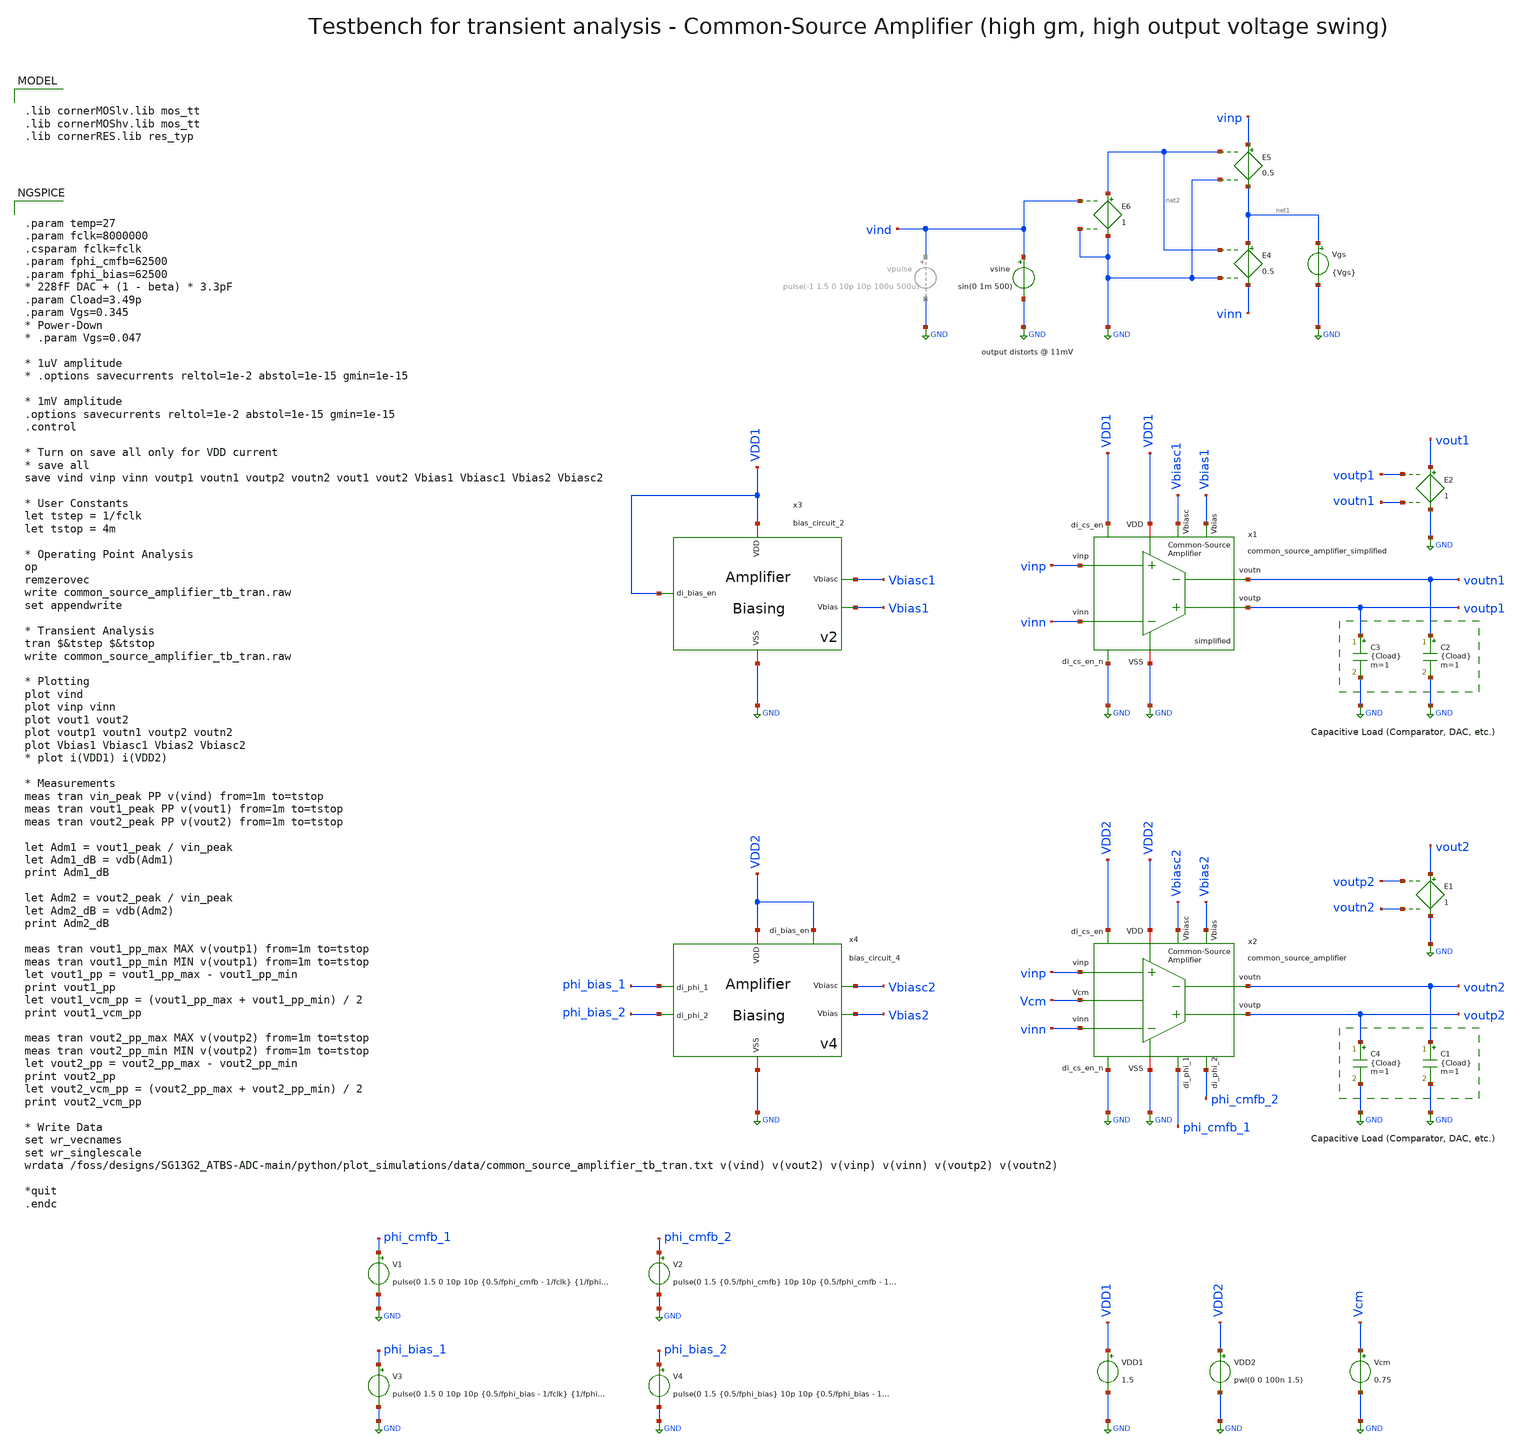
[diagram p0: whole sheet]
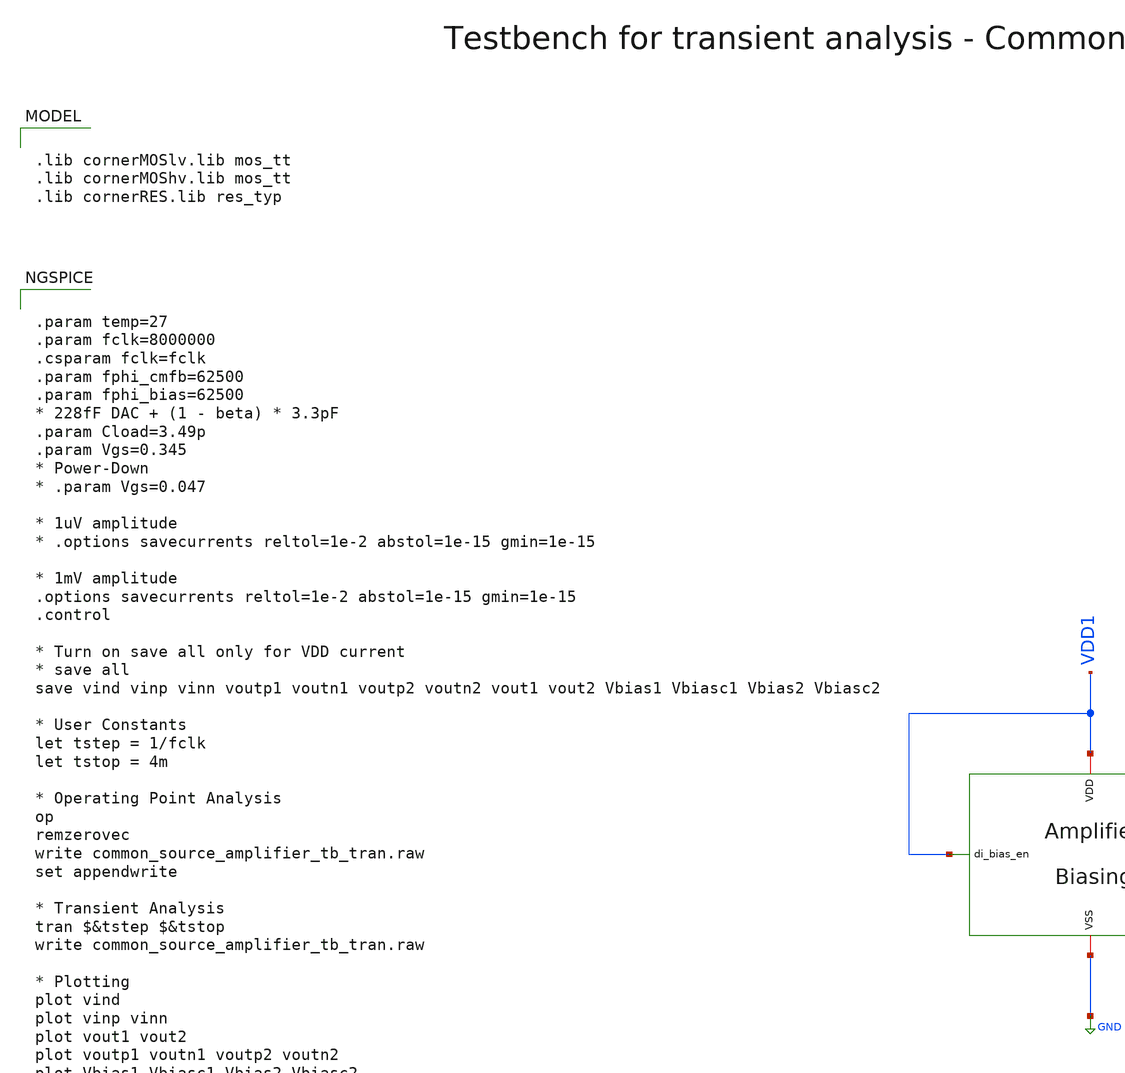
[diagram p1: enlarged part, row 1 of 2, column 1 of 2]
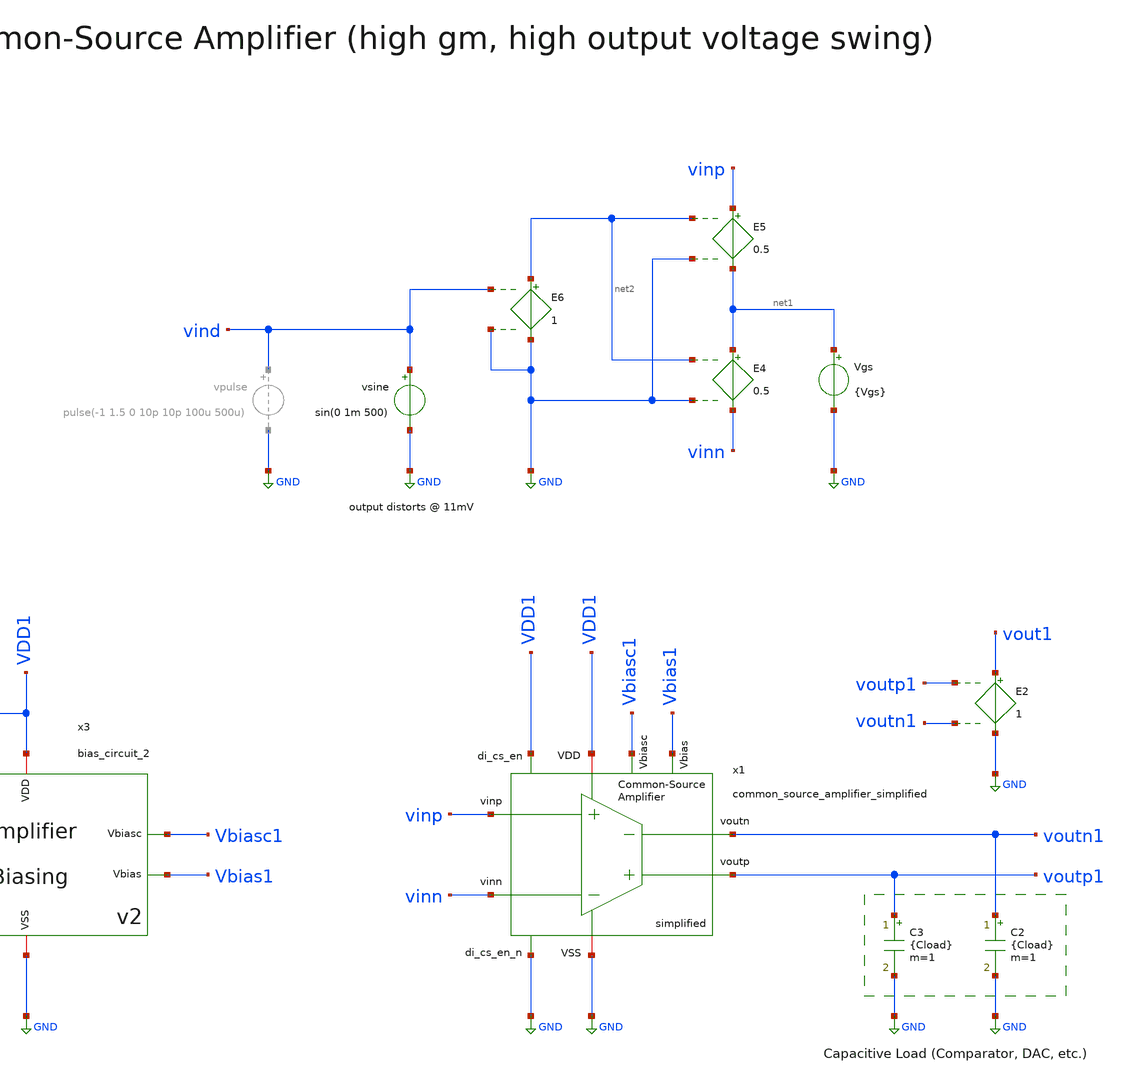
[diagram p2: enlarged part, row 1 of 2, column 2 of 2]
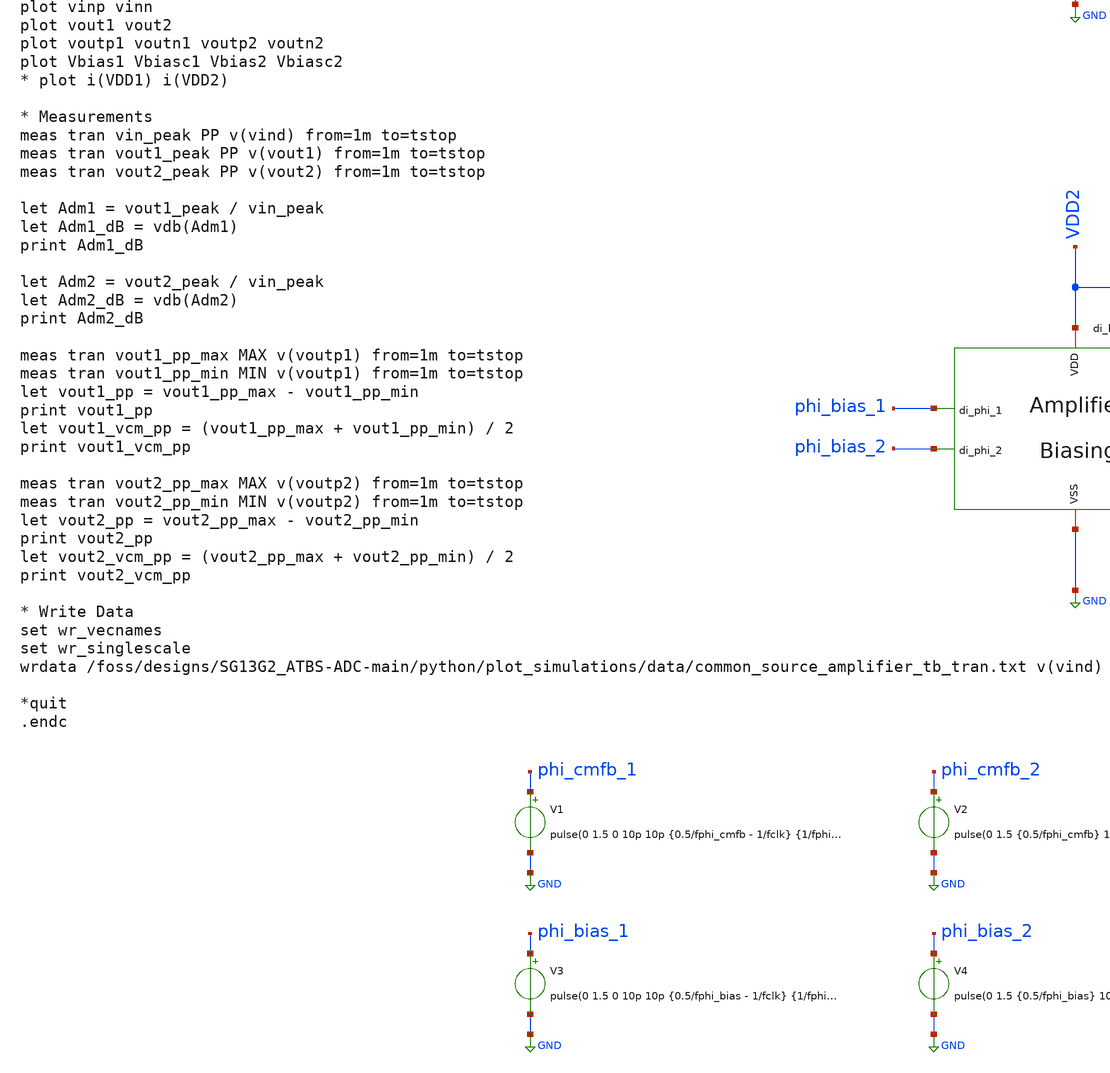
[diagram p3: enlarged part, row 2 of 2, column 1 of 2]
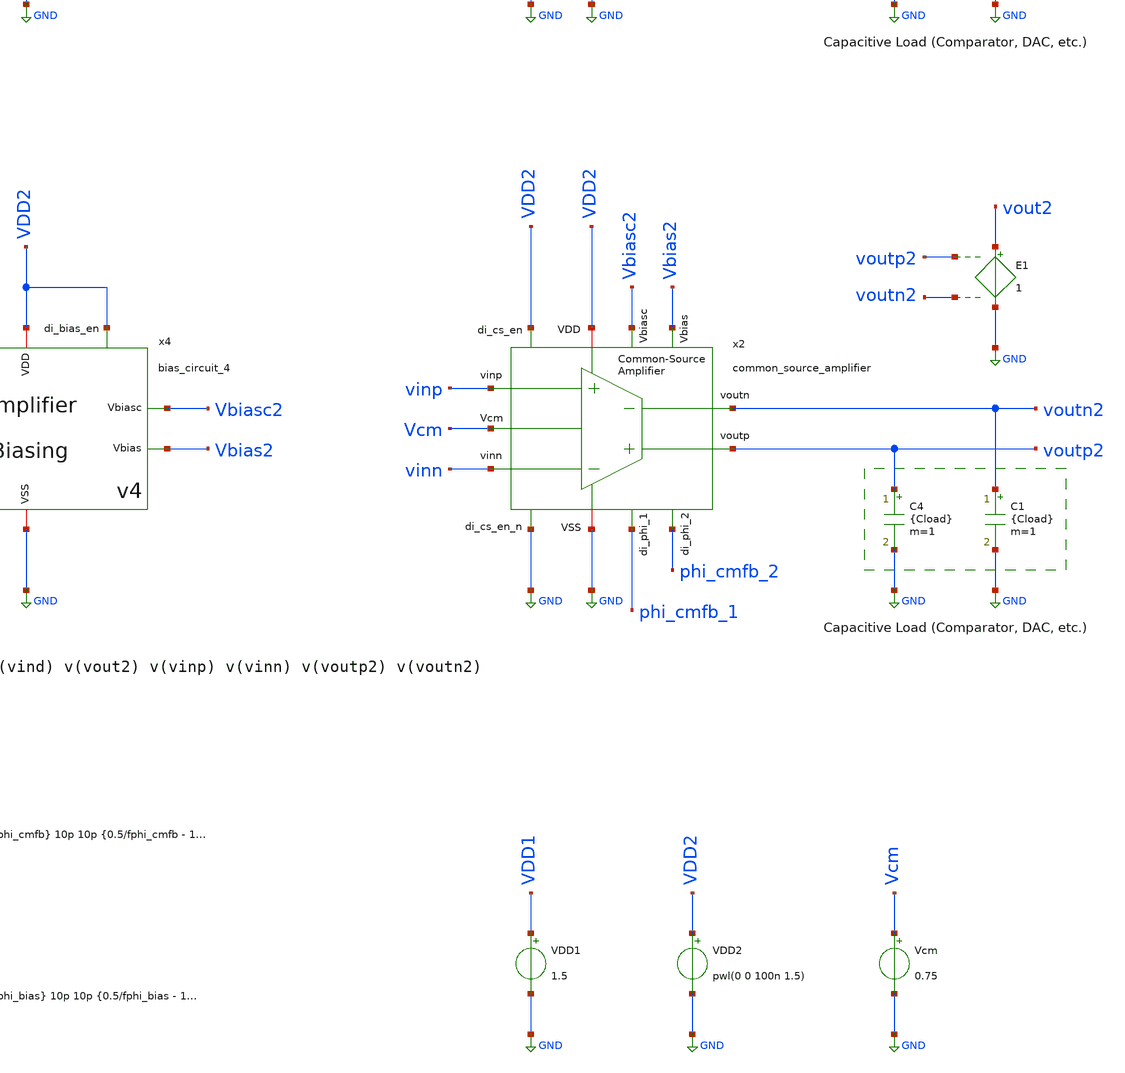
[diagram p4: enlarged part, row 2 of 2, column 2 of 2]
** sch_path: SG13G2_ATBS-ADC-main/xschem/bio_amplifier/amplifier_core/common_source_amplifier/testbenches/common_source_amplifier_tb_tran.sch
**.subckt common_source_amplifier_tb_tran
Vgs net1 GND {Vgs}
E4 net1 vinn net2 GND 0.5
E5 vinp net1 net2 GND 0.5
E6 net2 GND vind GND 1
C2 voutn1 GND {Cload} m=1
C3 voutp1 GND {Cload} m=1
E1 vout2 GND voutp2 voutn2 1
C1 voutn2 GND {Cload} m=1
C4 voutp2 GND {Cload} m=1
Vcm Vcm GND 0.75
E2 vout1 GND voutp1 voutn1 1
vsine vind GND sin(0 1m 500)
VDD1 VDD1 GND 1.5
x1 VDD1 voutp1 voutn1 vinn vinp GND VDD1 GND Vbiasc1 Vbias1 common_source_amplifier_simplified
x2 VDD2 voutp2 voutn2 vinn vinp GND Vcm phi_cmfb_1 phi_cmfb_2 VDD2 GND Vbiasc2 Vbias2
+ common_source_amplifier
x3 VDD1 Vbiasc1 VDD1 GND Vbias1 bias_circuit_2
V1 phi_cmfb_1 GND pulse(0 1.5 0 10p 10p {0.5/fphi_cmfb - 1/fclk} {1/fphi_cmfb})
V2 phi_cmfb_2 GND pulse(0 1.5 {0.5/fphi_cmfb} 10p 10p {0.5/fphi_cmfb - 1/fclk} {1/fphi_cmfb})
V3 phi_bias_1 GND pulse(0 1.5 0 10p 10p {0.5/fphi_bias - 1/fclk} {1/fphi_bias})
V4 phi_bias_2 GND pulse(0 1.5 {0.5/fphi_bias} 10p 10p {0.5/fphi_bias - 1/fclk} {1/fphi_bias})
x4 phi_bias_2 phi_bias_1 VDD2 GND Vbiasc2 Vbias2 VDD2 bias_circuit_4
VDD2 VDD2 GND pwl(0 0 100n 1.5)
**** begin user architecture code


.param temp=27
.param fclk=8000000
.csparam fclk=fclk
.param fphi_cmfb=62500
.param fphi_bias=62500
* 228fF DAC + (1 - beta) * 3.3pF
.param Cload=3.49p
.param Vgs=0.345
* Power-Down
* .param Vgs=0.047

* 1uV amplitude
* .options savecurrents reltol=1e-2 abstol=1e-15 gmin=1e-15

* 1mV amplitude
.options savecurrents reltol=1e-2 abstol=1e-15 gmin=1e-15
.control

* Turn on save all only for VDD current
* save all
save vind vinp vinn voutp1 voutn1 voutp2 voutn2 vout1 vout2 Vbias1 Vbiasc1 Vbias2 Vbiasc2

* User Constants
let tstep = 1/fclk
let tstop = 4m

* Operating Point Analysis
op
remzerovec
write common_source_amplifier_tb_tran.raw
set appendwrite

* Transient Analysis
tran $&tstep $&tstop
write common_source_amplifier_tb_tran.raw

* Plotting
plot vind
plot vinp vinn
plot vout1 vout2
plot voutp1 voutn1 voutp2 voutn2
plot Vbias1 Vbiasc1 Vbias2 Vbiasc2
* plot i(VDD1) i(VDD2)

* Measurements
meas tran vin_peak PP v(vind) from=1m to=tstop
meas tran vout1_peak PP v(vout1) from=1m to=tstop
meas tran vout2_peak PP v(vout2) from=1m to=tstop

let Adm1 = vout1_peak / vin_peak
let Adm1_dB = vdb(Adm1)
print Adm1_dB

let Adm2 = vout2_peak / vin_peak
let Adm2_dB = vdb(Adm2)
print Adm2_dB

meas tran vout1_pp_max MAX v(voutp1) from=1m to=tstop
meas tran vout1_pp_min MIN v(voutp1) from=1m to=tstop
let vout1_pp = vout1_pp_max - vout1_pp_min
print vout1_pp
let vout1_vcm_pp = (vout1_pp_max + vout1_pp_min) / 2
print vout1_vcm_pp

meas tran vout2_pp_max MAX v(voutp2) from=1m to=tstop
meas tran vout2_pp_min MIN v(voutp2) from=1m to=tstop
let vout2_pp = vout2_pp_max - vout2_pp_min
print vout2_pp
let vout2_vcm_pp = (vout2_pp_max + vout2_pp_min) / 2
print vout2_vcm_pp

* Write Data
set wr_vecnames
set wr_singlescale
wrdata
+ /foss/designs/SG13G2_ATBS-ADC-main/python/plot_simulations/data/common_source_amplifier_tb_tran.txt v(vind) v(vout2) v(vinp) v(vinn) v(voutp2) v(voutn2)

*quit
.endc



.lib cornerMOSlv.lib mos_tt
.lib cornerMOShv.lib mos_tt
.lib cornerRES.lib res_typ

**** end user architecture code
**.ends
.GLOBAL GND
.end
